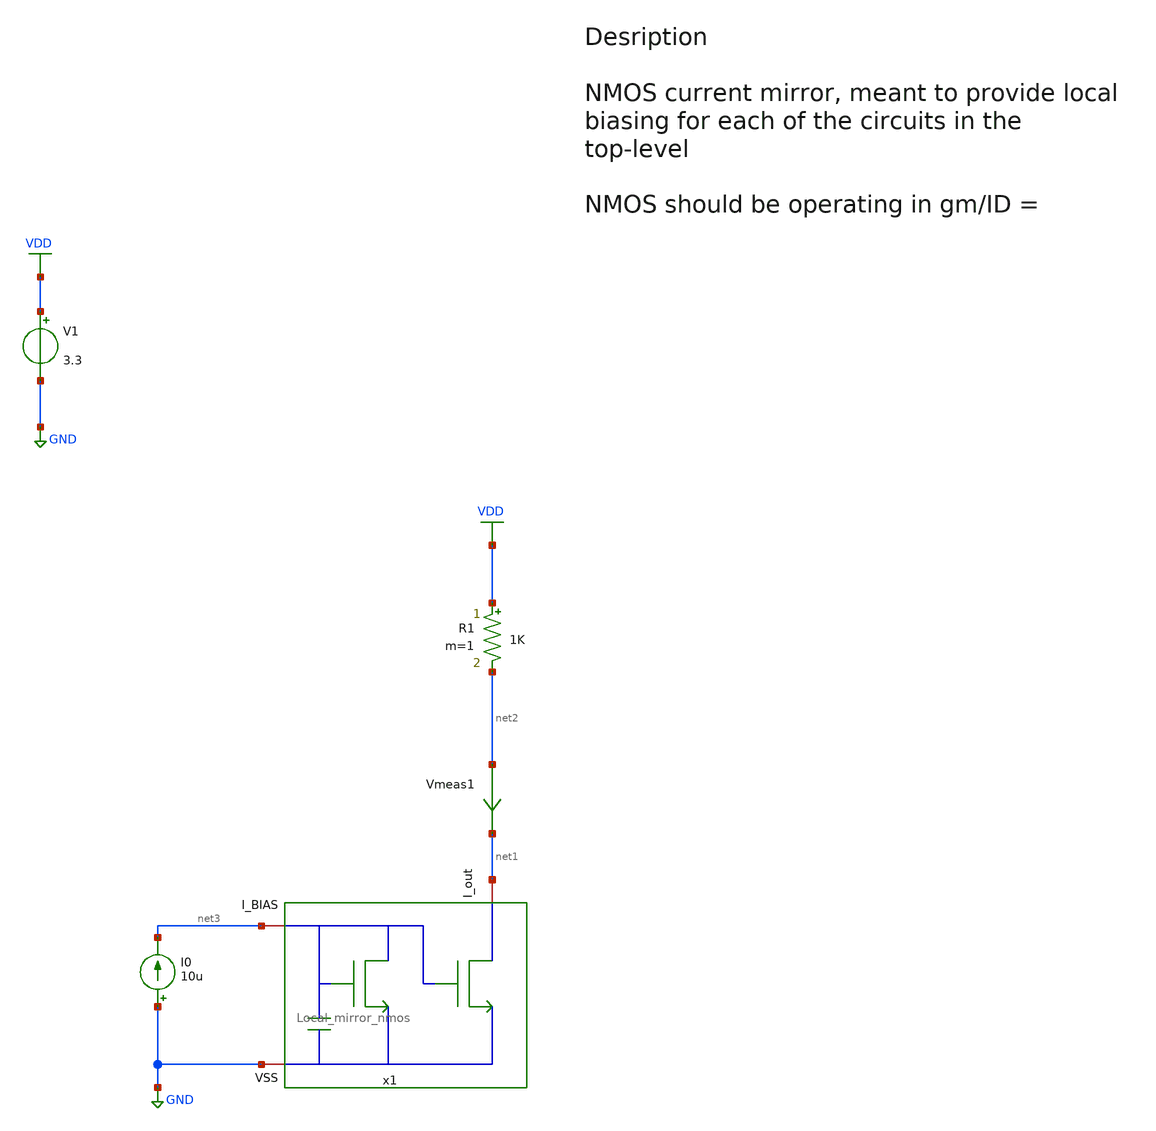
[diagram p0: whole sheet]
** sch_path: src/design_tb/Local_mirror_nmos_tb.sch
**.subckt Local_mirror_nmos_tb
I0 GND net3 10u
V1 VDD GND 3.3
.save i(v1)
Vmeas1 net2 net1 0
.save i(vmeas1)
R1 VDD net2 1K m=1
x1 net1 net3 GND Local_mirror_nmos l_ref=1u w_ref=1.5u l_mir=1u w_mir=8u
**** begin user architecture code

.include $::180MCU_MODELS/design.ngspice
.lib $::180MCU_MODELS/sm141064.ngspice typical
.lib $::180MCU_MODELS/sm141064.ngspice mimcap_typical
.lib $::180MCU_MODELS/sm141064.ngspice cap_mim
.lib $::180MCU_MODELS/sm141064.ngspice res_typical
.lib $::180MCU_MODELS/sm141064.ngspice diode_typical
.lib $::180MCU_MODELS/sm141064.ngspice bjt_typical
.lib $::180MCU_MODELS/sm141064.ngspice moscap_typical
.lib $::180MCU_MODELS/sm141064.ngspice mimcap_typical



* Add convergence aids
.option method=gear

.control

    * operating point
    op
    show

    write Local_mirror_nmos_tb.raw

    set appendwrite

    * Transient analysis to observe mixing operation
    tran 1n 0.01u
    write Local_mirror_nmos_tb.raw

.endc


**** end user architecture code
**.ends

* expanding   symbol:  /home/vasil/Downloads/SSCS_PICO_2025/src/design_xsch/Local_mirror_nmos.sym #
*+ of pins=3
** sym_path: src/design_xsch/Local_mirror_nmos.sym
** sch_path: src/design_xsch/Local_mirror_nmos.sch
.subckt Local_mirror_nmos I_out I_BIAS VSS    l_ref=1u w_ref=1u l_mir=1u w_mir=1u
*.iopin VSS
*.opin I_out
*.iopin I_BIAS
XM2 I_out I_BIAS VSS VSS nfet_03v3 L=l_mir W=w_mir nf=1 ad='int((nf+1)/2) * W/nf * 0.18u' as='int((nf+2)/2) * W/nf * 0.18u'
+ pd='2*int((nf+1)/2) * (W/nf + 0.18u)' ps='2*int((nf+2)/2) * (W/nf + 0.18u)' nrd='0.18u / W' nrs='0.18u / W'
+ sa=0 sb=0 sd=0 m=1
XM6 I_BIAS I_BIAS VSS VSS nfet_03v3 L=l_ref W=w_ref nf=1 ad='int((nf+1)/2) * W/nf * 0.18u' as='int((nf+2)/2) * W/nf * 0.18u'
+ pd='2*int((nf+1)/2) * (W/nf + 0.18u)' ps='2*int((nf+2)/2) * (W/nf + 0.18u)' nrd='0.18u / W' nrs='0.18u / W'
+ sa=0 sb=0 sd=0 m=1
XC1 I_BIAS VSS cap_mim_1f0fF c_width=1e-6 c_length=1e-6 m=1
.ends

.GLOBAL GND
.GLOBAL VDD
.end
